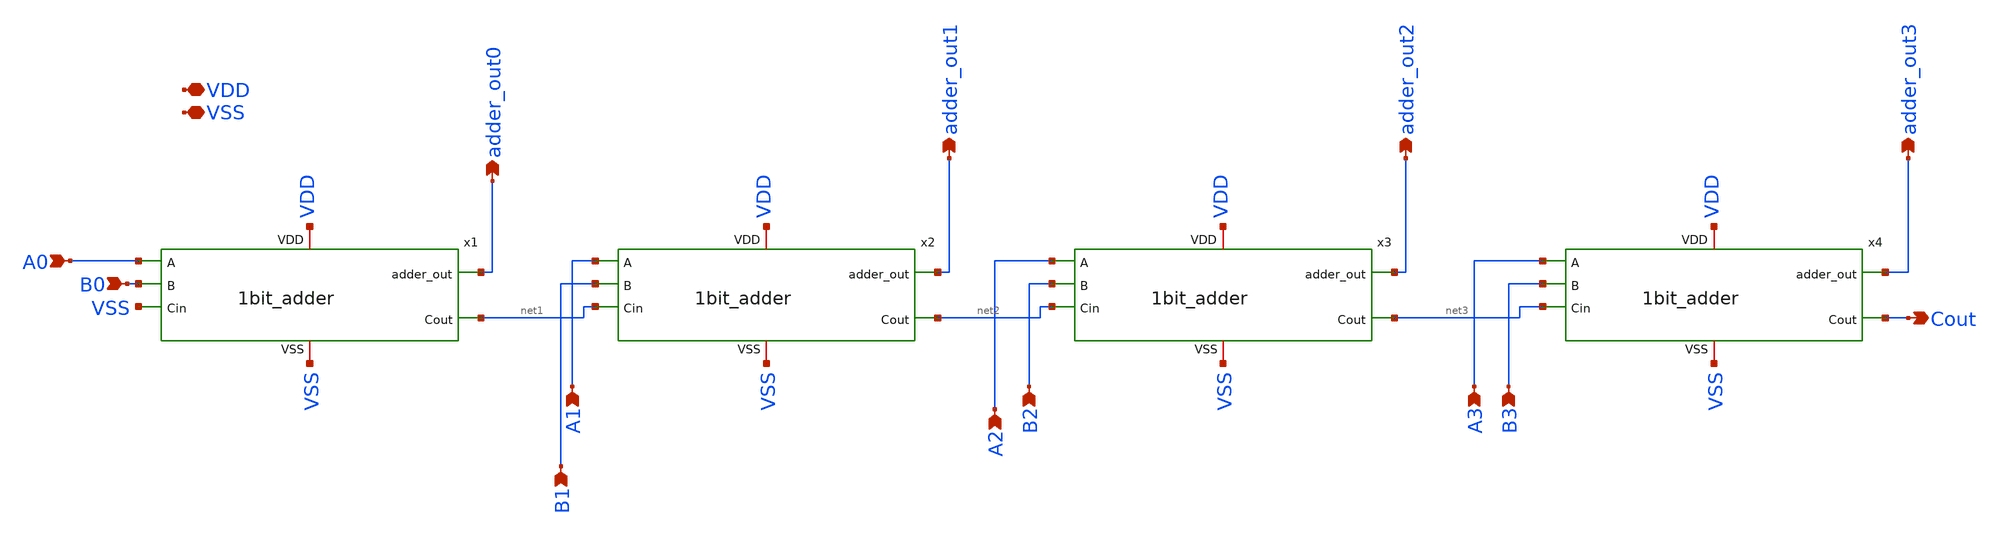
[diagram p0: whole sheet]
** sch_path: adder/4bit_adder.sch
**.subckt 4bit_adder VDD VSS B0 A1 B1 adder_out0 A2 B2 adder_out1 adder_out2 A3 B3 adder_out3 Cout
*+ A0
*.iopin VDD
*.iopin VSS
*.ipin B0
*.ipin A1
*.ipin B1
*.opin adder_out0
*.ipin A2
*.ipin B2
*.opin adder_out1
*.opin adder_out2
*.ipin A3
*.ipin B3
*.opin adder_out3
*.opin Cout
*.ipin A0
x1 VDD VSS A0 adder_out0 B0 net1 VSS 1bit_adder
x2 VDD VSS A1 adder_out1 B1 net2 net1 1bit_adder
x3 VDD VSS A2 adder_out2 B2 net3 net2 1bit_adder
x4 VDD VSS A3 adder_out3 B3 Cout net3 1bit_adder
**.ends

* expanding   symbol:  1bit_adder.sym # of pins=7
** sym_path: adder/1bit_adder.sym
** sch_path: adder/1bit_adder.sch
.subckt 1bit_adder VDD VSS A adder_out B Cout Cin
*.ipin A
*.ipin B
*.iopin VDD
*.iopin VSS
*.ipin Cin
*.opin Cout
*.opin adder_out
x1 A B VDD VSS net1 xor2
x2 VSS VDD A net2 B and2
x3 VSS VDD net1 net3 Cin and2
x4 net1 Cin VDD VSS adder_out xor2
x5 net3 net2 VDD VSS Cout xor2
x6 net1 Cin VDD VSS adder_out xor2
.ends


* expanding   symbol:  xor2/xor2.sym # of pins=5
** sym_path: xor2/xor2.sym
** sch_path: xor2/xor2.sch
.subckt xor2 A B VDD VSS out
*.ipin A
*.ipin B
*.opin out
*.ipin VDD
*.ipin VSS
XM1 out notA net3 net3 sky130_fd_pr__nfet_01v8 L=0.15 W=1 nf=1 ad='int((nf+1)/2) * W/nf * 0.29' as='int((nf+2)/2) * W/nf * 0.29'
+ pd='2*int((nf+1)/2) * (W/nf + 0.29)' ps='2*int((nf+2)/2) * (W/nf + 0.29)' nrd='0.29 / W' nrs='0.29 / W'
+ sa=0 sb=0 sd=0 mult=1 m=1
XM2 out B net1 net1 sky130_fd_pr__pfet_01v8 L=0.15 W=1 nf=1 ad='int((nf+1)/2) * W/nf * 0.29' as='int((nf+2)/2) * W/nf * 0.29'
+ pd='2*int((nf+1)/2) * (W/nf + 0.29)' ps='2*int((nf+2)/2) * (W/nf + 0.29)' nrd='0.29 / W' nrs='0.29 / W'
+ sa=0 sb=0 sd=0 mult=1 m=1
XM3 net3 notB VSS VSS sky130_fd_pr__nfet_01v8 L=0.15 W=1 nf=1 ad='int((nf+1)/2) * W/nf * 0.29' as='int((nf+2)/2) * W/nf * 0.29'
+ pd='2*int((nf+1)/2) * (W/nf + 0.29)' ps='2*int((nf+2)/2) * (W/nf + 0.29)' nrd='0.29 / W' nrs='0.29 / W'
+ sa=0 sb=0 sd=0 mult=1 m=1
XM4 net1 notA VDD VDD sky130_fd_pr__pfet_01v8 L=0.15 W=1 nf=1 ad='int((nf+1)/2) * W/nf * 0.29' as='int((nf+2)/2) * W/nf * 0.29'
+ pd='2*int((nf+1)/2) * (W/nf + 0.29)' ps='2*int((nf+2)/2) * (W/nf + 0.29)' nrd='0.29 / W' nrs='0.29 / W'
+ sa=0 sb=0 sd=0 mult=1 m=1
XM5 net4 A VDD VDD sky130_fd_pr__pfet_01v8 L=0.15 W=1 nf=1 ad='int((nf+1)/2) * W/nf * 0.29' as='int((nf+2)/2) * W/nf * 0.29'
+ pd='2*int((nf+1)/2) * (W/nf + 0.29)' ps='2*int((nf+2)/2) * (W/nf + 0.29)' nrd='0.29 / W' nrs='0.29 / W'
+ sa=0 sb=0 sd=0 mult=1 m=1
XM6 out notB net4 net4 sky130_fd_pr__pfet_01v8 L=0.15 W=1 nf=1 ad='int((nf+1)/2) * W/nf * 0.29' as='int((nf+2)/2) * W/nf * 0.29'
+ pd='2*int((nf+1)/2) * (W/nf + 0.29)' ps='2*int((nf+2)/2) * (W/nf + 0.29)' nrd='0.29 / W' nrs='0.29 / W'
+ sa=0 sb=0 sd=0 mult=1 m=1
XM7 out A net2 net2 sky130_fd_pr__nfet_01v8 L=0.15 W=1 nf=1 ad='int((nf+1)/2) * W/nf * 0.29' as='int((nf+2)/2) * W/nf * 0.29'
+ pd='2*int((nf+1)/2) * (W/nf + 0.29)' ps='2*int((nf+2)/2) * (W/nf + 0.29)' nrd='0.29 / W' nrs='0.29 / W'
+ sa=0 sb=0 sd=0 mult=1 m=1
XM8 net2 B VSS VSS sky130_fd_pr__nfet_01v8 L=0.15 W=1 nf=1 ad='int((nf+1)/2) * W/nf * 0.29' as='int((nf+2)/2) * W/nf * 0.29'
+ pd='2*int((nf+1)/2) * (W/nf + 0.29)' ps='2*int((nf+2)/2) * (W/nf + 0.29)' nrd='0.29 / W' nrs='0.29 / W'
+ sa=0 sb=0 sd=0 mult=1 m=1
XM9 notA A VDD VDD sky130_fd_pr__pfet_01v8 L=0.15 W=1 nf=1 ad='int((nf+1)/2) * W/nf * 0.29' as='int((nf+2)/2) * W/nf * 0.29'
+ pd='2*int((nf+1)/2) * (W/nf + 0.29)' ps='2*int((nf+2)/2) * (W/nf + 0.29)' nrd='0.29 / W' nrs='0.29 / W'
+ sa=0 sb=0 sd=0 mult=1 m=1
XM10 notA A VSS VSS sky130_fd_pr__nfet_01v8 L=0.15 W=1 nf=1 ad='int((nf+1)/2) * W/nf * 0.29' as='int((nf+2)/2) * W/nf * 0.29'
+ pd='2*int((nf+1)/2) * (W/nf + 0.29)' ps='2*int((nf+2)/2) * (W/nf + 0.29)' nrd='0.29 / W' nrs='0.29 / W'
+ sa=0 sb=0 sd=0 mult=1 m=1
XM11 notB B VDD VDD sky130_fd_pr__pfet_01v8 L=0.15 W=1 nf=1 ad='int((nf+1)/2) * W/nf * 0.29' as='int((nf+2)/2) * W/nf * 0.29'
+ pd='2*int((nf+1)/2) * (W/nf + 0.29)' ps='2*int((nf+2)/2) * (W/nf + 0.29)' nrd='0.29 / W' nrs='0.29 / W'
+ sa=0 sb=0 sd=0 mult=1 m=1
XM12 notB B VSS VSS sky130_fd_pr__nfet_01v8 L=0.15 W=1 nf=1 ad='int((nf+1)/2) * W/nf * 0.29' as='int((nf+2)/2) * W/nf * 0.29'
+ pd='2*int((nf+1)/2) * (W/nf + 0.29)' ps='2*int((nf+2)/2) * (W/nf + 0.29)' nrd='0.29 / W' nrs='0.29 / W'
+ sa=0 sb=0 sd=0 mult=1 m=1
.ends


* expanding   symbol:  and/and2.sym # of pins=5
** sym_path: and/and2.sym
** sch_path: and/and2.sch
.subckt and2 VSS VDD A out B
*.ipin VDD
*.ipin A
*.ipin B
*.ipin VSS
*.opin out
XM1 net1 A net2 net2 sky130_fd_pr__nfet_01v8 L=0.15 W=1 nf=1 ad='int((nf+1)/2) * W/nf * 0.29' as='int((nf+2)/2) * W/nf * 0.29'
+ pd='2*int((nf+1)/2) * (W/nf + 0.29)' ps='2*int((nf+2)/2) * (W/nf + 0.29)' nrd='0.29 / W' nrs='0.29 / W'
+ sa=0 sb=0 sd=0 mult=1 m=1
XM2 net1 A VDD VDD sky130_fd_pr__pfet_01v8 L=0.15 W=1 nf=1 ad='int((nf+1)/2) * W/nf * 0.29' as='int((nf+2)/2) * W/nf * 0.29'
+ pd='2*int((nf+1)/2) * (W/nf + 0.29)' ps='2*int((nf+2)/2) * (W/nf + 0.29)' nrd='0.29 / W' nrs='0.29 / W'
+ sa=0 sb=0 sd=0 mult=1 m=1
XM3 net2 B VSS VSS sky130_fd_pr__nfet_01v8 L=0.15 W=1 nf=1 ad='int((nf+1)/2) * W/nf * 0.29' as='int((nf+2)/2) * W/nf * 0.29'
+ pd='2*int((nf+1)/2) * (W/nf + 0.29)' ps='2*int((nf+2)/2) * (W/nf + 0.29)' nrd='0.29 / W' nrs='0.29 / W'
+ sa=0 sb=0 sd=0 mult=1 m=1
XM4 net1 B VDD VDD sky130_fd_pr__pfet_01v8 L=0.15 W=1 nf=1 ad='int((nf+1)/2) * W/nf * 0.29' as='int((nf+2)/2) * W/nf * 0.29'
+ pd='2*int((nf+1)/2) * (W/nf + 0.29)' ps='2*int((nf+2)/2) * (W/nf + 0.29)' nrd='0.29 / W' nrs='0.29 / W'
+ sa=0 sb=0 sd=0 mult=1 m=1
XM5 out net1 VDD VDD sky130_fd_pr__pfet_01v8 L=0.15 W=1 nf=1 ad='int((nf+1)/2) * W/nf * 0.29' as='int((nf+2)/2) * W/nf * 0.29'
+ pd='2*int((nf+1)/2) * (W/nf + 0.29)' ps='2*int((nf+2)/2) * (W/nf + 0.29)' nrd='0.29 / W' nrs='0.29 / W'
+ sa=0 sb=0 sd=0 mult=1 m=1
XM6 out net1 VSS VSS sky130_fd_pr__nfet_01v8 L=0.15 W=1 nf=1 ad='int((nf+1)/2) * W/nf * 0.29' as='int((nf+2)/2) * W/nf * 0.29'
+ pd='2*int((nf+1)/2) * (W/nf + 0.29)' ps='2*int((nf+2)/2) * (W/nf + 0.29)' nrd='0.29 / W' nrs='0.29 / W'
+ sa=0 sb=0 sd=0 mult=1 m=1
.ends

.end
